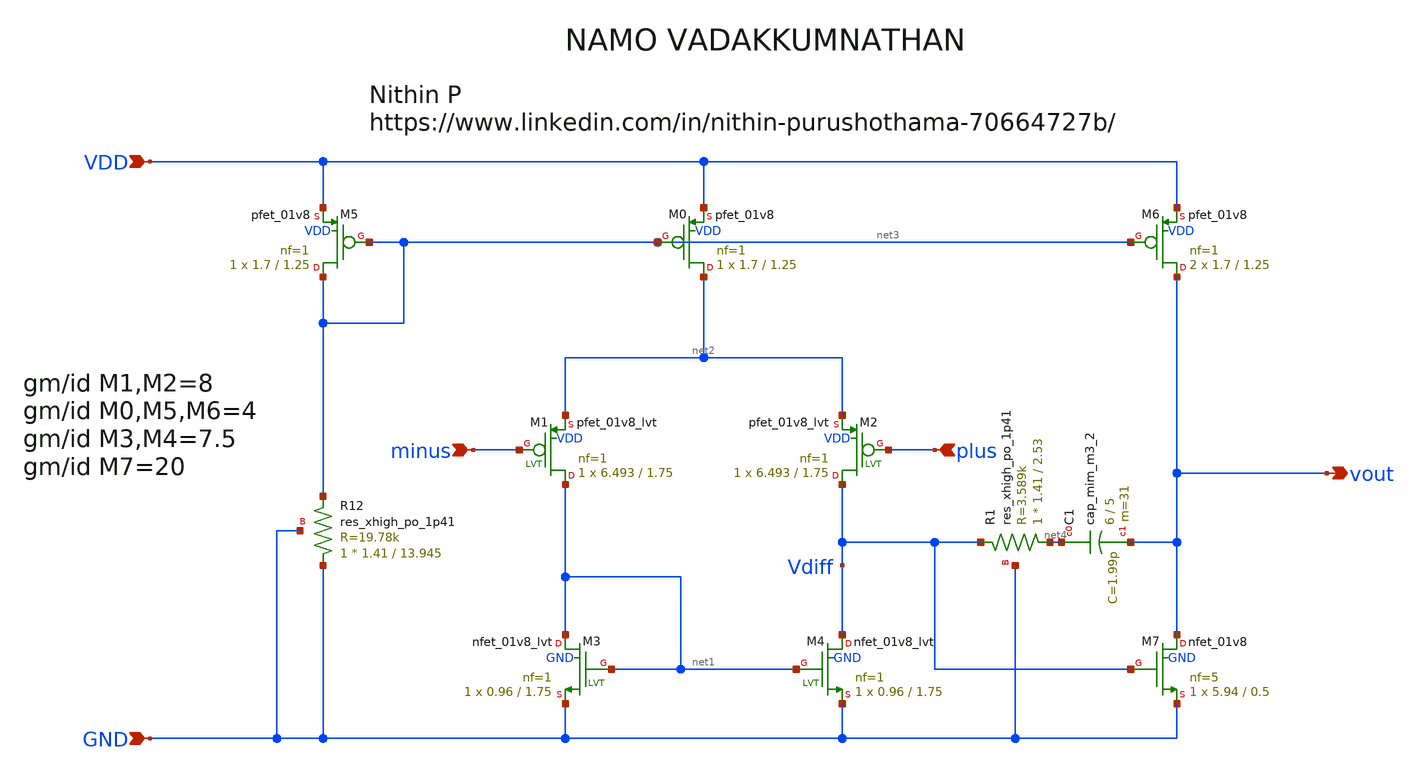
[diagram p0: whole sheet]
** sch_path: Schematic/OTA.sch
**.subckt OTA VDD GND minus plus vout
*.ipin VDD
*.ipin GND
*.ipin minus
*.ipin plus
*.opin vout
XM3 net1 net1 GND GND sky130_fd_pr__nfet_01v8_lvt L=1.75 W=0.96 nf=1 ad='int((nf+1)/2) * W/nf * 0.29'
+ as='int((nf+2)/2) * W/nf * 0.29' pd='2*int((nf+1)/2) * (W/nf + 0.29)' ps='2*int((nf+2)/2) * (W/nf + 0.29)'
+ nrd='0.29 / W' nrs='0.29 / W' sa=0 sb=0 sd=0 mult=1 m=1
XM1 net1 minus net2 VDD sky130_fd_pr__pfet_01v8_lvt L=1.75 W=6.493 nf=1 ad='int((nf+1)/2) * W/nf * 0.29'
+ as='int((nf+2)/2) * W/nf * 0.29' pd='2*int((nf+1)/2) * (W/nf + 0.29)' ps='2*int((nf+2)/2) * (W/nf + 0.29)'
+ nrd='0.29 / W' nrs='0.29 / W' sa=0 sb=0 sd=0 mult=1 m=1
XM4 Vdiff net1 GND GND sky130_fd_pr__nfet_01v8_lvt L=1.75 W=0.96 nf=1 ad='int((nf+1)/2) * W/nf * 0.29'
+ as='int((nf+2)/2) * W/nf * 0.29' pd='2*int((nf+1)/2) * (W/nf + 0.29)' ps='2*int((nf+2)/2) * (W/nf + 0.29)'
+ nrd='0.29 / W' nrs='0.29 / W' sa=0 sb=0 sd=0 mult=1 m=1
XM2 Vdiff plus net2 VDD sky130_fd_pr__pfet_01v8_lvt L=1.75 W=6.493 nf=1 ad='int((nf+1)/2) * W/nf * 0.29'
+ as='int((nf+2)/2) * W/nf * 0.29' pd='2*int((nf+1)/2) * (W/nf + 0.29)' ps='2*int((nf+2)/2) * (W/nf + 0.29)'
+ nrd='0.29 / W' nrs='0.29 / W' sa=0 sb=0 sd=0 mult=1 m=1
XM0 net2 net3 VDD VDD sky130_fd_pr__pfet_01v8 L=1.25 W=1.7 nf=1 ad='int((nf+1)/2) * W/nf * 0.29' as='int((nf+2)/2) * W/nf * 0.29'
+ pd='2*int((nf+1)/2) * (W/nf + 0.29)' ps='2*int((nf+2)/2) * (W/nf + 0.29)' nrd='0.29 / W' nrs='0.29 / W'
+ sa=0 sb=0 sd=0 mult=1 m=1
XM5 net3 net3 VDD VDD sky130_fd_pr__pfet_01v8 L=1.25 W=1.7 nf=1 ad='int((nf+1)/2) * W/nf * 0.29' as='int((nf+2)/2) * W/nf * 0.29'
+ pd='2*int((nf+1)/2) * (W/nf + 0.29)' ps='2*int((nf+2)/2) * (W/nf + 0.29)' nrd='0.29 / W' nrs='0.29 / W'
+ sa=0 sb=0 sd=0 mult=1 m=1
XM6 vout net3 VDD VDD sky130_fd_pr__pfet_01v8 L=1.25 W=1.7 nf=1 ad='int((nf+1)/2) * W/nf * 0.29' as='int((nf+2)/2) * W/nf * 0.29'
+ pd='2*int((nf+1)/2) * (W/nf + 0.29)' ps='2*int((nf+2)/2) * (W/nf + 0.29)' nrd='0.29 / W' nrs='0.29 / W'
+ sa=0 sb=0 sd=0 mult=2 m=2
XM7 vout Vdiff GND GND sky130_fd_pr__nfet_01v8 L=0.5 W=5.94 nf=5 ad='int((nf+1)/2) * W/nf * 0.29' as='int((nf+2)/2) * W/nf * 0.29'
+ pd='2*int((nf+1)/2) * (W/nf + 0.29)' ps='2*int((nf+2)/2) * (W/nf + 0.29)' nrd='0.29 / W' nrs='0.29 / W'
+ sa=0 sb=0 sd=0 mult=1 m=1
XR12 GND net3 GND sky130_fd_pr__res_xhigh_po_1p41 L=13.945 mult=1 m=1
XR1 net4 Vdiff GND sky130_fd_pr__res_xhigh_po_1p41 L=2.53 mult=1 m=1
XC1 net4 vout sky130_fd_pr__cap_mim_m3_2 W=6 L=5 MF=31 m=31
**.ends
.end
